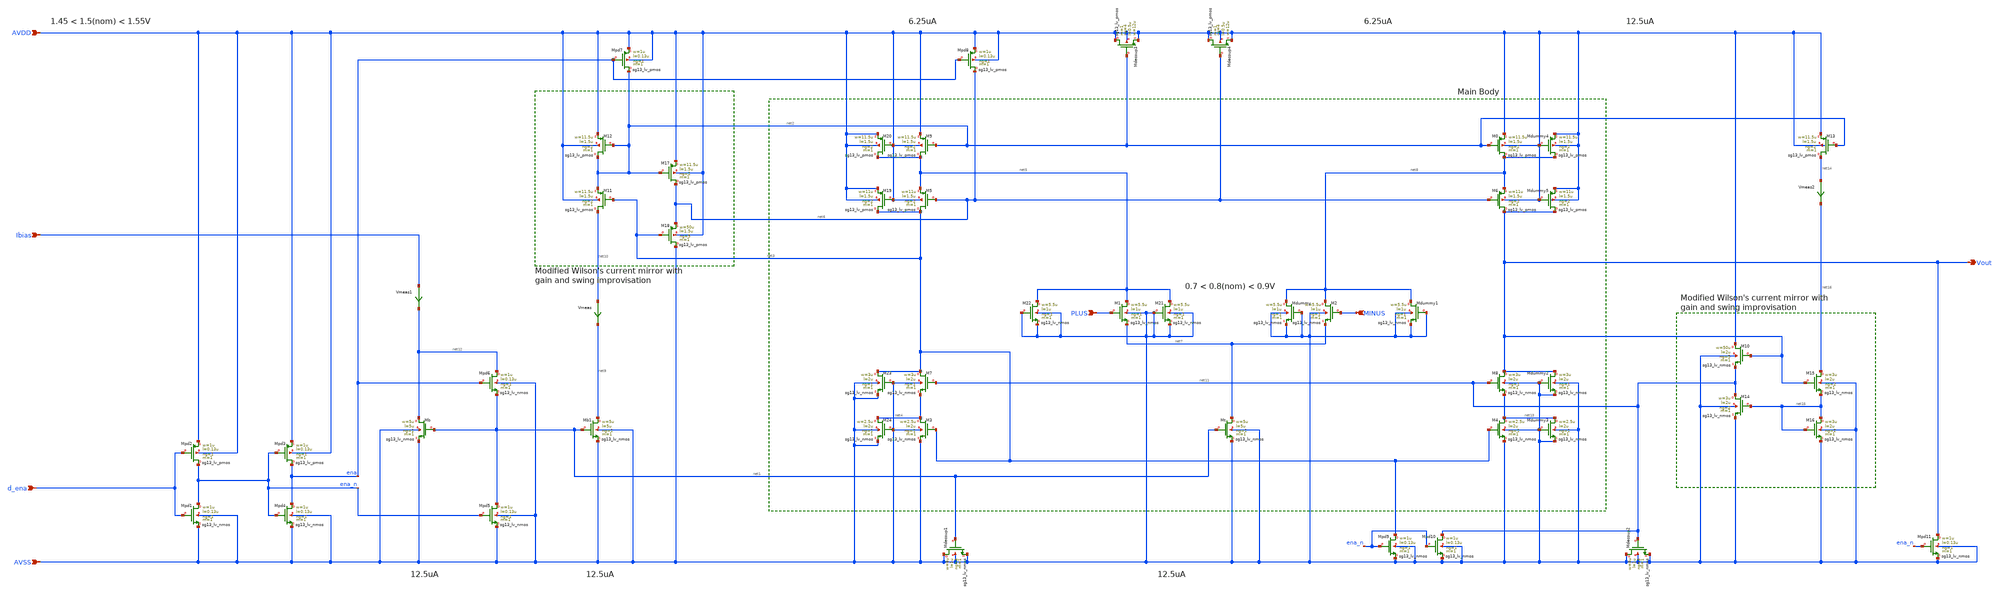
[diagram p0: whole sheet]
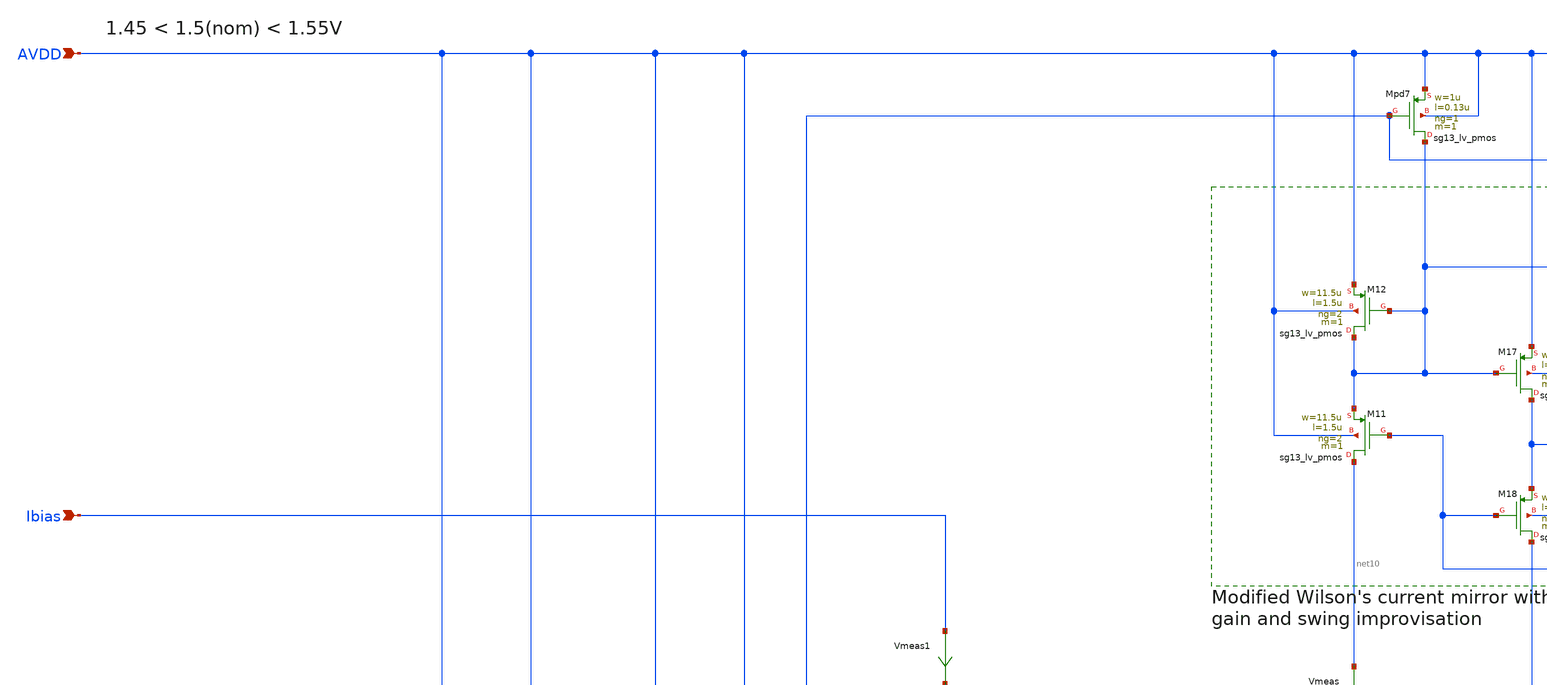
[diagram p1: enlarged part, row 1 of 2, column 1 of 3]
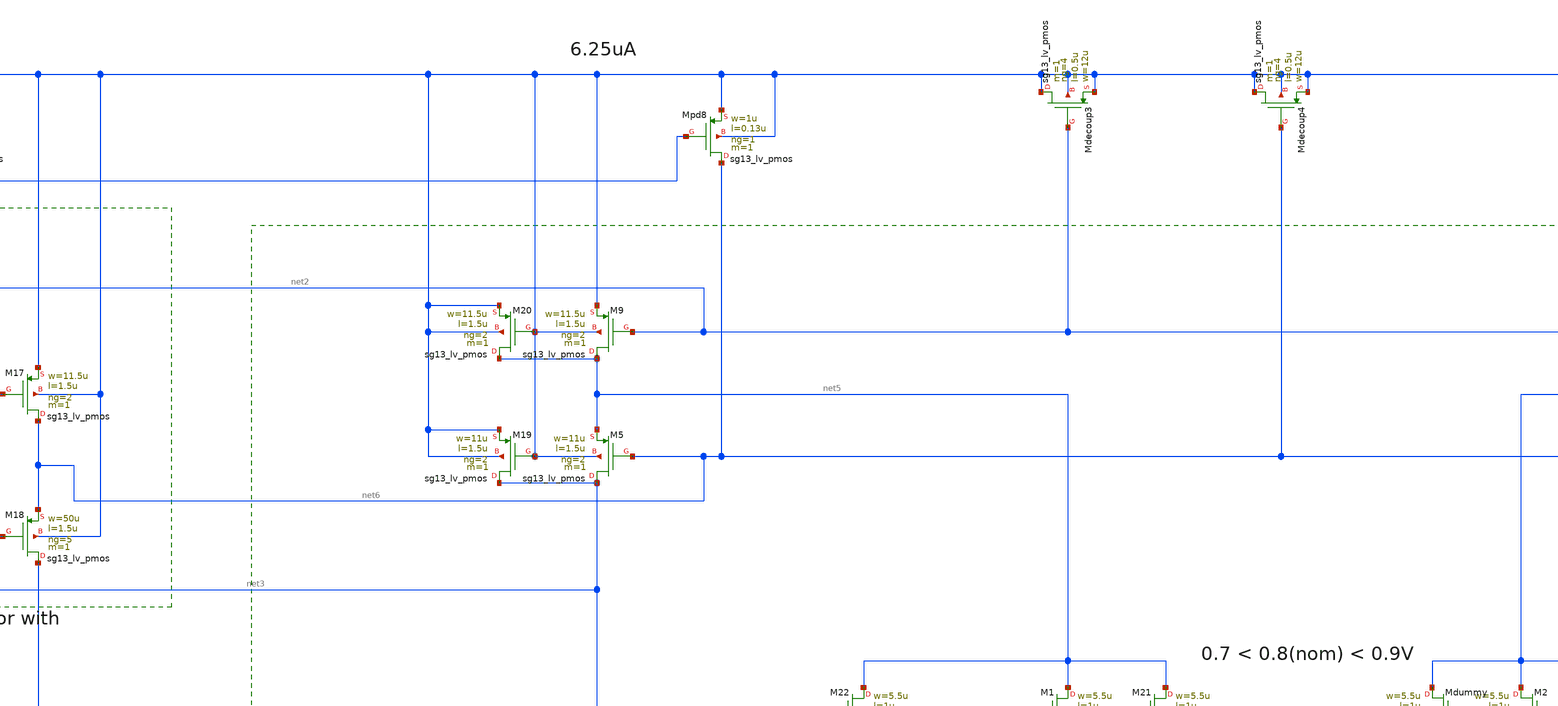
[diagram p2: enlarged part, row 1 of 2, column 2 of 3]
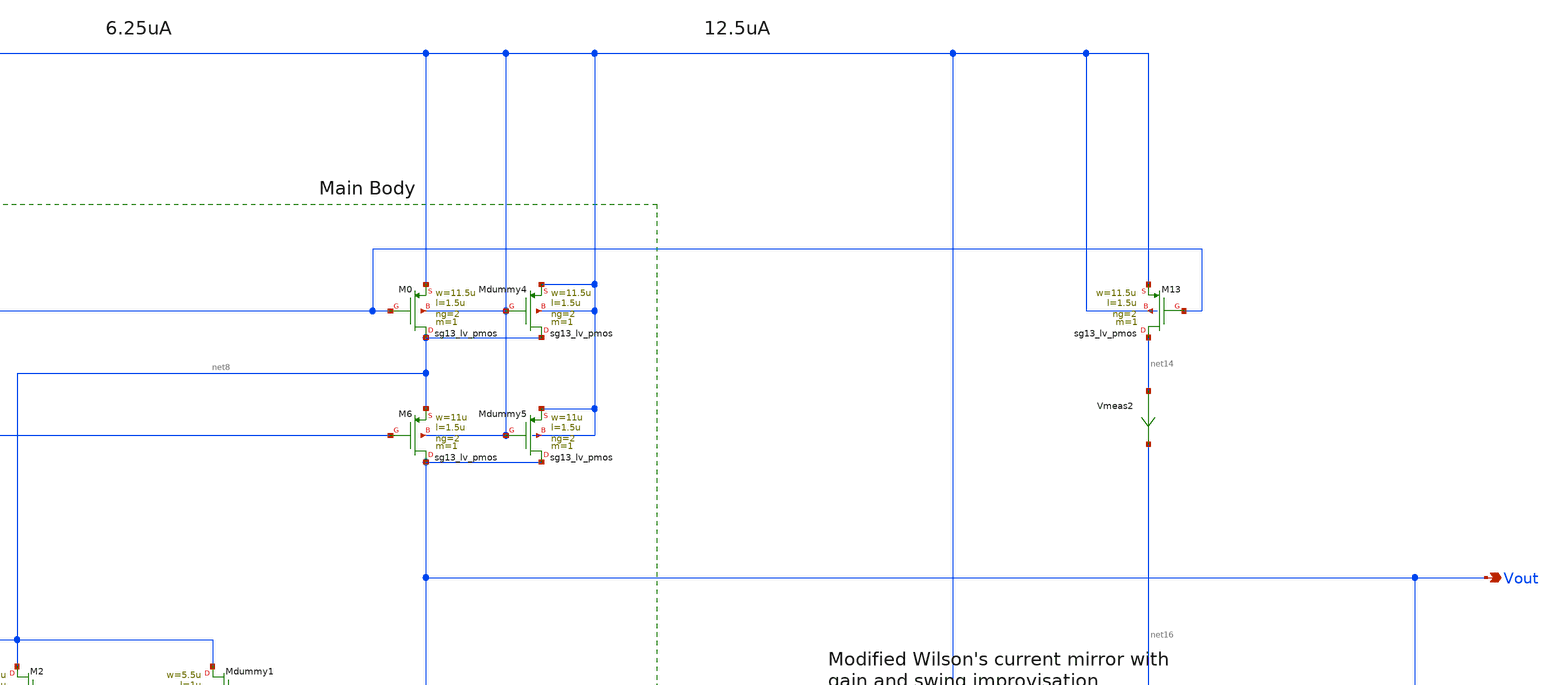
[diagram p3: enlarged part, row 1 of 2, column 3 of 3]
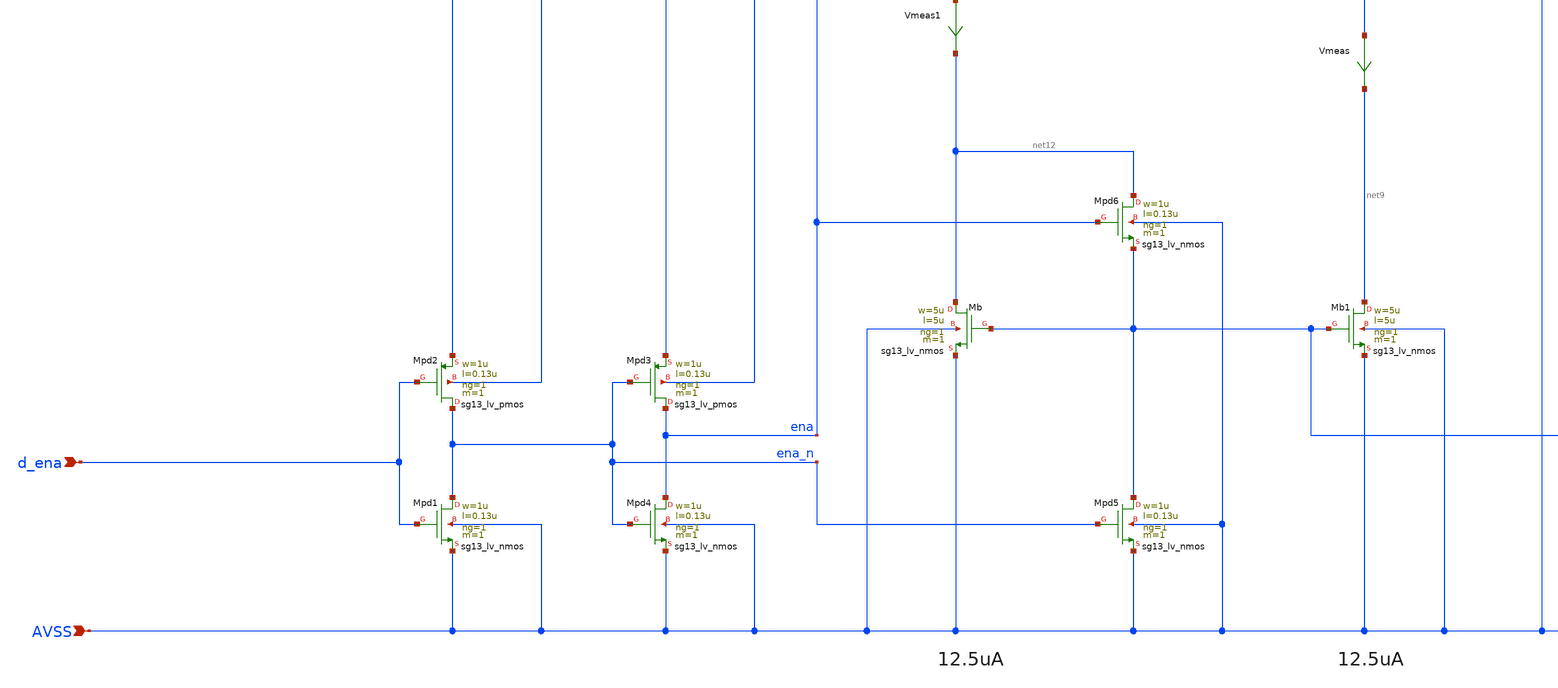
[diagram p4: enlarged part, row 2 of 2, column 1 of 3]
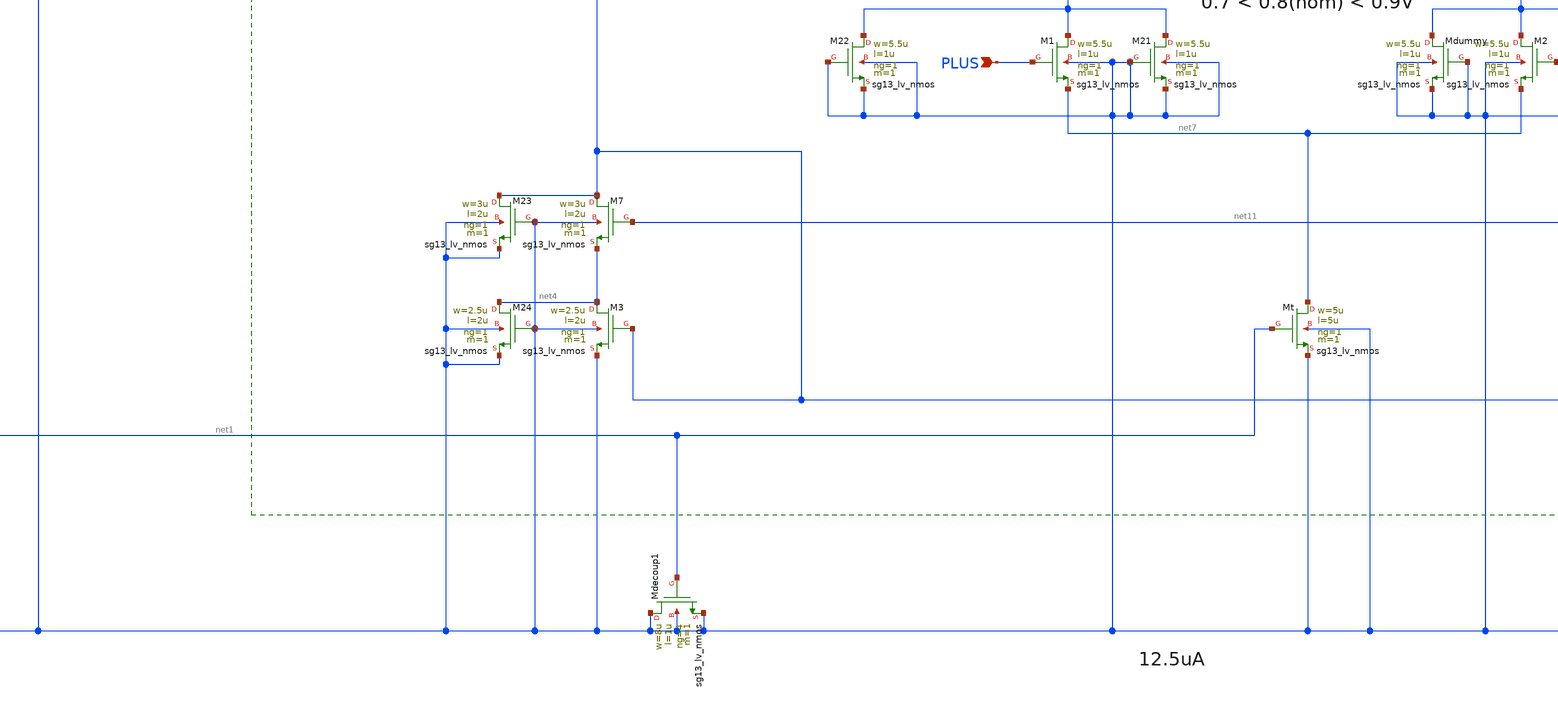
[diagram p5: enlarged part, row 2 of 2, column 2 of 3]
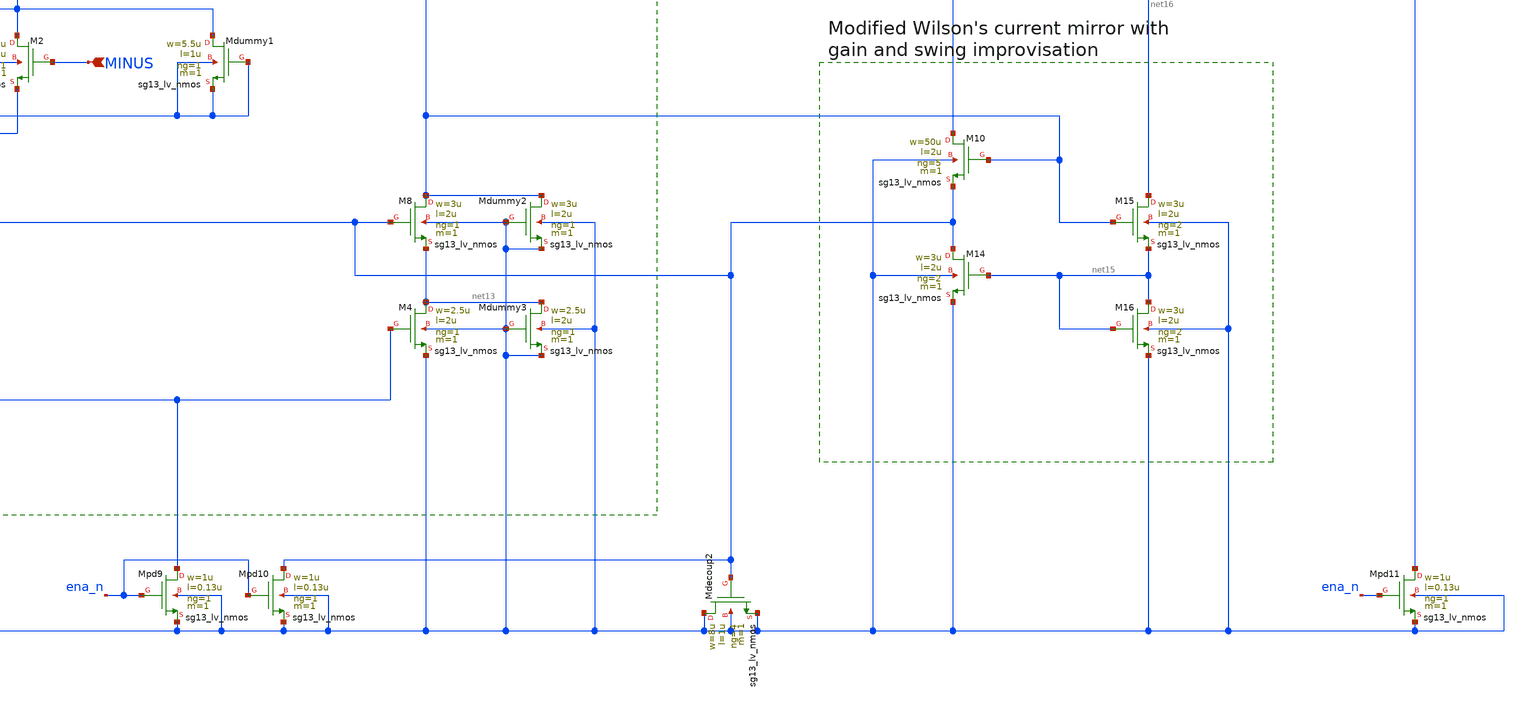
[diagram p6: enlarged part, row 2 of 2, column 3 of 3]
** sch_path: Designs/otas/1_schematics/foldedcascode_nmos_withdummies.sch
* (c) 2025 Thesis_HP, Apache-2.0 license
**.subckt foldedcascode_nmos_withdummies AVSS Ibias AVDD PLUS MINUS Vout d_ena
*.ipin AVSS
*.ipin Ibias
*.ipin AVDD
*.ipin PLUS
*.ipin MINUS
*.opin Vout
*.ipin d_ena
XMb net12 net1 AVSS AVSS sg13_lv_nmos w=5u l=5u ng=1 m=1 mm_ok=1
XMpd5 net1 ena_n AVSS AVSS sg13_lv_nmos w=1u l=0.13u ng=1 m=1 mm_ok=1
XMpd6 net12 ena net1 AVSS sg13_lv_nmos w=1u l=0.13u ng=1 m=1 mm_ok=1
XMb1 net9 net1 AVSS AVSS sg13_lv_nmos w=5u l=5u ng=1 m=1 mm_ok=1
Vmeas net10 net9 0
.save i(vmeas)
XM11 net10 net3 net2 AVDD sg13_lv_pmos w=11.5u l=1.5u ng=2 m=1 mm_ok=1
XM12 net2 net2 AVDD AVDD sg13_lv_pmos w=11.5u l=1.5u ng=2 m=1 mm_ok=1
XM18 AVSS net3 net6 AVDD sg13_lv_pmos w=50u l=1.5u ng=5 m=1 mm_ok=1
XM17 net6 net2 AVDD AVDD sg13_lv_pmos w=11.5u l=1.5u ng=2 m=1 mm_ok=1
XM9 net5 net2 AVDD AVDD sg13_lv_pmos w=11.5u l=1.5u ng=2 m=1 mm_ok=1
XM5 net3 net6 net5 AVDD sg13_lv_pmos w=11u l=1.5u ng=2 m=1 mm_ok=1
XM7 net3 net11 net4 AVSS sg13_lv_nmos w=3u l=2u ng=1 m=1 mm_ok=1
XM3 net4 net3 AVSS AVSS sg13_lv_nmos w=2.5u l=2u ng=1 m=1 mm_ok=1
XMpd7 net2 ena AVDD AVDD sg13_lv_pmos w=1u l=0.13u ng=1 m=1 mm_ok=1
XMpd8 net6 ena AVDD AVDD sg13_lv_pmos w=1u l=0.13u ng=1 m=1 mm_ok=1
XMt net7 net1 AVSS AVSS sg13_lv_nmos w=5u l=5u ng=1 m=1 mm_ok=1
XM1 net5 PLUS net7 AVSS sg13_lv_nmos w=5.5u l=1u ng=1 m=1 mm_ok=1
XM2 net8 MINUS net7 AVSS sg13_lv_nmos w=5.5u l=1u ng=1 m=1 mm_ok=1
XMdecoup3 AVDD net2 AVDD AVDD sg13_lv_pmos w=12u l=0.5u ng=4 m=1 mm_ok=1
XMdecoup4 AVDD net6 AVDD AVDD sg13_lv_pmos w=12u l=0.5u ng=4 m=1 mm_ok=1
XMdecoup1 AVSS net1 AVSS AVSS sg13_lv_nmos w=8u l=1u ng=4 m=1 mm_ok=1
XMpd2 ena_n d_ena AVDD AVDD sg13_lv_pmos w=1u l=0.13u ng=1 m=1 mm_ok=1
Vmeas1 Ibias net12 0
.save i(vmeas1)
XMpd3 ena ena_n AVDD AVDD sg13_lv_pmos w=1u l=0.13u ng=1 m=1 mm_ok=1
XMpd1 ena_n d_ena AVSS AVSS sg13_lv_nmos w=1u l=0.13u ng=1 m=1 mm_ok=1
XMpd4 ena ena_n AVSS AVSS sg13_lv_nmos w=1u l=0.13u ng=1 m=1 mm_ok=1
XMdummy net8 AVSS AVSS AVSS sg13_lv_nmos w=5.5u l=1u ng=1 m=1 mm_ok=1
XMdummy1 net8 AVSS AVSS AVSS sg13_lv_nmos w=5.5u l=1u ng=1 m=1 mm_ok=1
XM6 Vout net6 net8 AVDD sg13_lv_pmos w=11u l=1.5u ng=2 m=1 mm_ok=1
XM0 net8 net2 AVDD AVDD sg13_lv_pmos w=11.5u l=1.5u ng=2 m=1 mm_ok=1
XM8 Vout net11 net13 AVSS sg13_lv_nmos w=3u l=2u ng=1 m=1 mm_ok=1
XM4 net13 net3 AVSS AVSS sg13_lv_nmos w=2.5u l=2u ng=1 m=1 mm_ok=1
XMdummy3 net13 AVSS AVSS AVSS sg13_lv_nmos w=2.5u l=2u ng=1 m=1 mm_ok=1
XMdummy2 Vout AVSS AVSS AVSS sg13_lv_nmos w=3u l=2u ng=1 m=1 mm_ok=1
XMdummy4 net8 AVDD AVDD AVDD sg13_lv_pmos w=11.5u l=1.5u ng=2 m=1 mm_ok=1
XMdummy5 Vout AVDD AVDD AVDD sg13_lv_pmos w=11u l=1.5u ng=2 m=1 mm_ok=1
XM13 net14 net2 AVDD AVDD sg13_lv_pmos w=11.5u l=1.5u ng=2 m=1 mm_ok=1
Vmeas2 net14 net16 0
.save i(vmeas2)
XM15 net16 Vout net15 AVSS sg13_lv_nmos w=3u l=2u ng=2 m=1 mm_ok=1
XM16 net15 net15 AVSS AVSS sg13_lv_nmos w=3u l=2u ng=2 m=1 mm_ok=1
XM14 net11 net15 AVSS AVSS sg13_lv_nmos w=3u l=2u ng=2 m=1 mm_ok=1
XM10 AVDD Vout net11 AVSS sg13_lv_nmos w=50u l=2u ng=5 m=1 mm_ok=1
XMpd11 Vout ena_n AVSS AVSS sg13_lv_nmos w=1u l=0.13u ng=1 m=1 mm_ok=1
XMdecoup2 AVSS net11 AVSS AVSS sg13_lv_nmos w=8u l=1u ng=4 m=1 mm_ok=1
XMpd10 net11 ena_n AVSS AVSS sg13_lv_nmos w=1u l=0.13u ng=1 m=1 mm_ok=1
XMpd9 net3 ena_n AVSS AVSS sg13_lv_nmos w=1u l=0.13u ng=1 m=1 mm_ok=1
XM19 net3 AVDD AVDD AVDD sg13_lv_pmos w=11u l=1.5u ng=2 m=1 mm_ok=1
XM20 net5 AVDD AVDD AVDD sg13_lv_pmos w=11.5u l=1.5u ng=2 m=1 mm_ok=1
XM21 net5 AVSS AVSS AVSS sg13_lv_nmos w=5.5u l=1u ng=1 m=1 mm_ok=1
XM22 net5 AVSS AVSS AVSS sg13_lv_nmos w=5.5u l=1u ng=1 m=1 mm_ok=1
XM23 net3 AVSS AVSS AVSS sg13_lv_nmos w=3u l=2u ng=1 m=1 mm_ok=1
XM24 net4 AVSS AVSS AVSS sg13_lv_nmos w=2.5u l=2u ng=1 m=1 mm_ok=1
**.ends
.end
